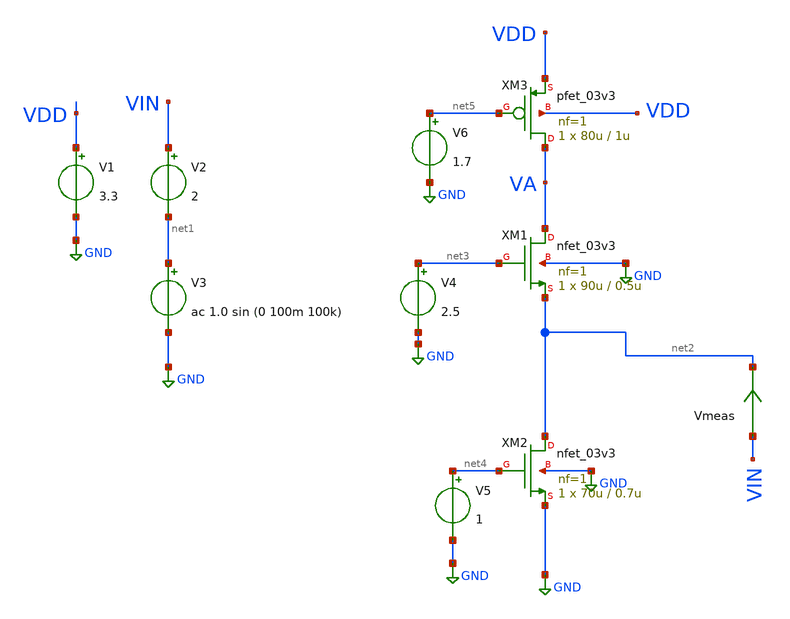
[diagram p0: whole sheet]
** sch_path: output_impedance/output_impedance5.sch
**.subckt output_impedance5
V1 VDD GND 3.3
V2 VIN net1 2
Vmeas VIN net2 0
.save i(vmeas)
V3 net1 GND ac 1.0 sin (0 100m 100k)
XM1 VA net3 net2 GND nfet_03v3 L=0.5u W=90u nf=1 ad='int((nf+1)/2) * W/nf * 0.18u' as='int((nf+2)/2) * W/nf * 0.18u'
+ pd='2*int((nf+1)/2) * (W/nf + 0.18u)' ps='2*int((nf+2)/2) * (W/nf + 0.18u)' nrd='0.18u / W' nrs='0.18u / W'
+ sa=0 sb=0 sd=0 m=1
V4 net3 GND 2.5
XM2 net2 net4 GND GND nfet_03v3 L=0.7u W=70u nf=1 ad='int((nf+1)/2) * W/nf * 0.18u' as='int((nf+2)/2) * W/nf * 0.18u'
+ pd='2*int((nf+1)/2) * (W/nf + 0.18u)' ps='2*int((nf+2)/2) * (W/nf + 0.18u)' nrd='0.18u / W' nrs='0.18u / W'
+ sa=0 sb=0 sd=0 m=1
V5 net4 GND 1
XM3 VA net5 VDD VDD pfet_03v3 L=1u W=80u nf=1 ad='int((nf+1)/2) * W/nf * 0.18u' as='int((nf+2)/2) * W/nf * 0.18u'
+ pd='2*int((nf+1)/2) * (W/nf + 0.18u)' ps='2*int((nf+2)/2) * (W/nf + 0.18u)' nrd='0.18u / W' nrs='0.18u / W'
+ sa=0 sb=0 sd=0 m=1
V6 net5 GND 1.7
**** begin user architecture code

.include $::180MCU_MODELS/design.ngspice
*.lib $::180MCU_MODELS/sm141064.ngspice statistical
*.lib $::180MCU_MODELS/sm141064.ngspice res_statistical
.lib $::180MCU_MODELS/sm141064.ngspice typical
.lib $::180MCU_MODELS/sm141064.ngspice res_typical
.lib $::180MCU_MODELS/sm141064.ngspice moscap_typical
.lib $::180MCU_MODELS/sm141064.ngspice bjt_typical
.lib $::180MCU_MODELS/sm141064.ngspice diode_typical
.lib $::180MCU_MODELS/sm141064.ngspice mimcap_typical
.TEMP 27

.param   sw_stat_global = 1   sw_stat_mism = 1  mc_skew = 3  res_mc_skew = 3  cap_mc_skew = 3
+  fnoicor = 1



.control
save all
dc V2 0 3.3 0.01
plot v(Va)

plot i(Vmeas) 1/(deriv(i(Vmeas)))
plot i(Vmeas)
plot deriv(v(VOUT))
tran 100n 10u
plot i(Vmeas)
.endc

**** end user architecture code
**.ends
.GLOBAL GND
.end
